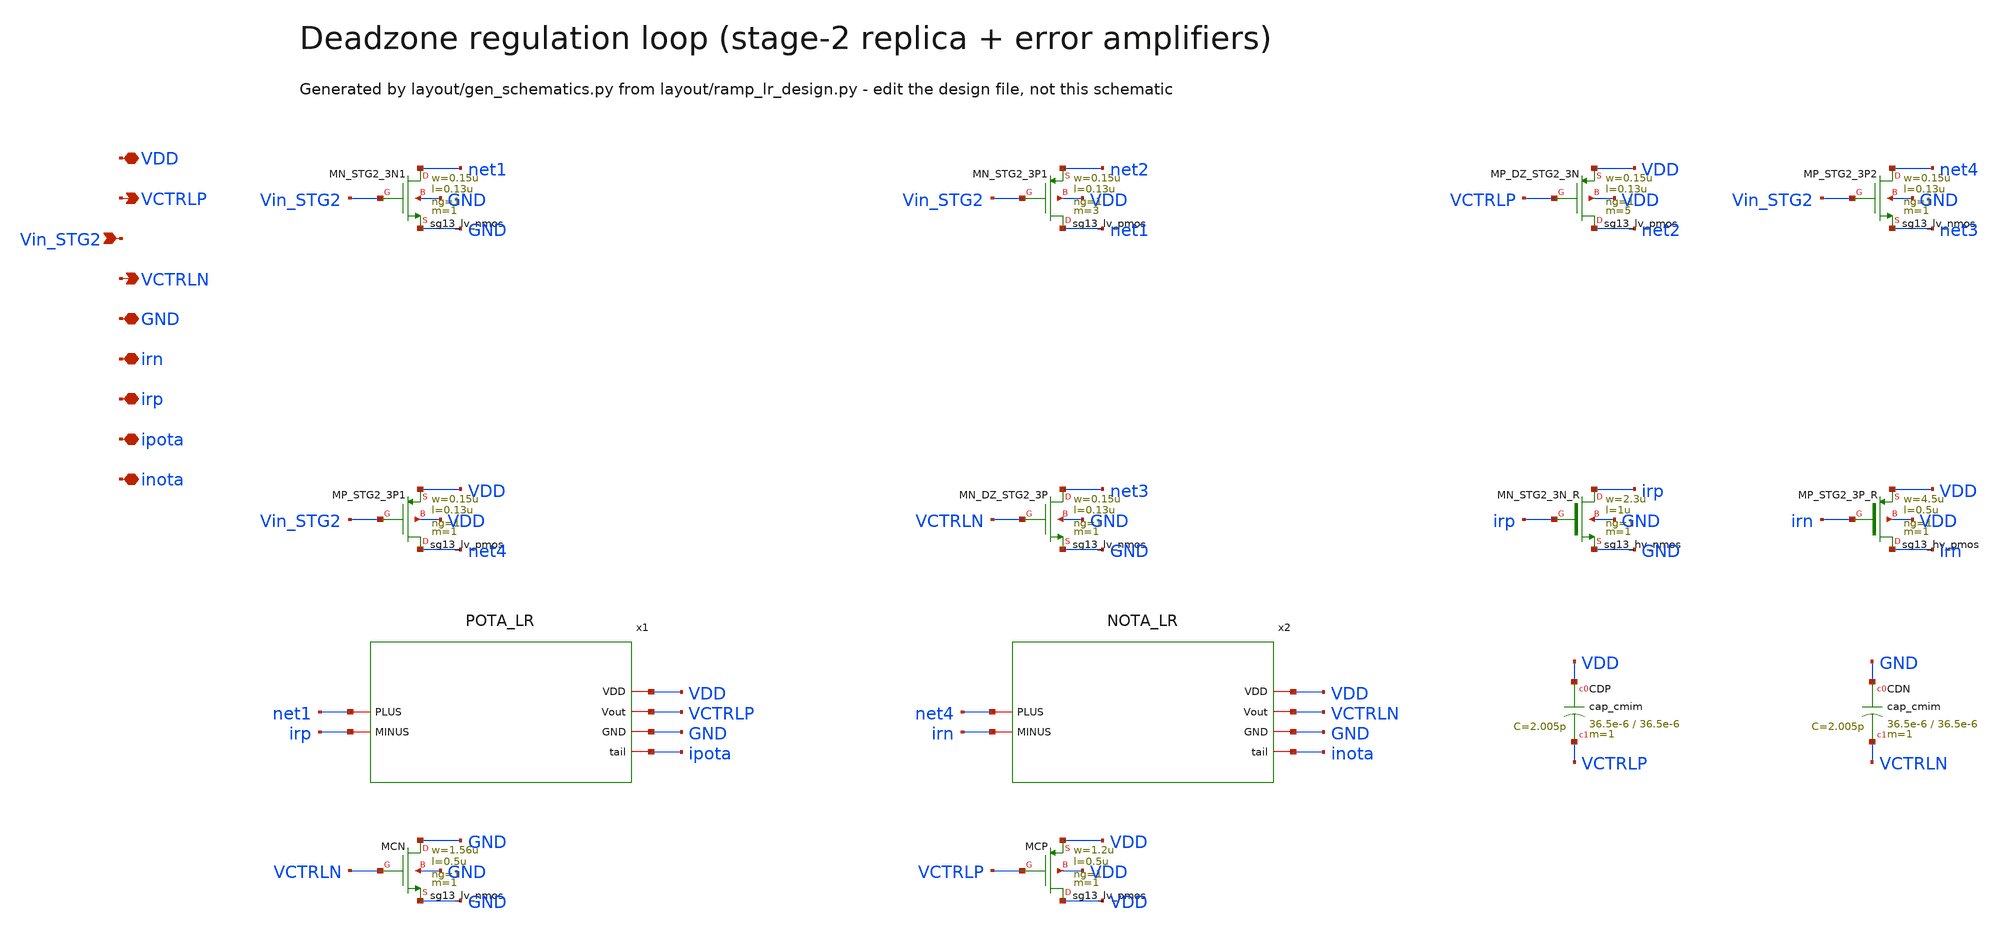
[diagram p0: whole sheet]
** sch_path: Design Files/RAMP/RAMP-LR/STG2_REPLICA_LR.sch
**.subckt STG2_REPLICA_LR VDD VCTRLP Vin_STG2 VCTRLN GND irn irp ipota inota
*.iopin VDD
*.opin VCTRLP
*.ipin Vin_STG2
*.opin VCTRLN
*.iopin GND
*.iopin irn
*.iopin irp
*.iopin ipota
*.iopin inota
XMN_STG2_3N1 net1 Vin_STG2 GND GND sg13_lv_nmos w=0.15u l=0.13u ng=1 m=1 mm_ok=1
XMN_STG2_3P1 net1 Vin_STG2 net2 VDD sg13_lv_pmos w=0.15u l=0.13u ng=1 m=3 mm_ok=1
XMP_DZ_STG2_3N net2 VCTRLP VDD VDD sg13_lv_pmos w=0.15u l=0.13u ng=1 m=5 mm_ok=1
XMP_STG2_3P2 net4 Vin_STG2 net3 GND sg13_lv_nmos w=0.15u l=0.13u ng=1 m=1 mm_ok=1
XMP_STG2_3P1 net4 Vin_STG2 VDD VDD sg13_lv_pmos w=0.15u l=0.13u ng=1 m=1 mm_ok=1
XMN_DZ_STG2_3P net3 VCTRLN GND GND sg13_lv_nmos w=0.15u l=0.13u ng=1 m=1 mm_ok=1
XMN_STG2_3N_R irp irp GND GND sg13_hv_nmos w=2.3u l=1u ng=1 m=1 mm_ok=1
XMP_STG2_3P_R irn irn VDD VDD sg13_hv_pmos w=4.5u l=0.5u ng=1 m=1 mm_ok=1
x1 VDD net1 irp VCTRLP GND ipota POTA_LR
x2 VDD VCTRLN net4 irn GND inota NOTA_LR
XCDP VDD VCTRLP cap_cmim w=36.5e-6 l=36.5e-6 m=1 mm_ok=1
XCDN GND VCTRLN cap_cmim w=36.5e-6 l=36.5e-6 m=1 mm_ok=1
XMCN GND VCTRLN GND GND sg13_lv_nmos w=1.56u l=0.5u ng=1 m=1 mm_ok=1
XMCP VDD VCTRLP VDD VDD sg13_lv_pmos w=1.2u l=0.5u ng=1 m=1 mm_ok=1
**.ends

* expanding   symbol:  RAMP-LR/POTA_LR.sym # of pins=6
** sym_path: Design Files/RAMP/RAMP-LR/POTA_LR.sym
** sch_path: Design Files/RAMP/RAMP-LR/POTA_LR.sch
.subckt POTA_LR VDD PLUS MINUS Vout GND tail
*.iopin VDD
*.ipin PLUS
*.ipin MINUS
*.opin Vout
*.iopin GND
*.iopin tail
XM2 net2 PLUS tail VDD sg13_lv_pmos w=1.2u l=0.5u ng=1 m=2 mm_ok=1
XM1 Vout MINUS tail VDD sg13_lv_pmos w=1.2u l=0.5u ng=1 m=2 mm_ok=1
XM4 Vout net2 GND GND sg13_hv_nmos w=0.5u l=2u ng=1 m=2 mm_ok=1
XM5 net2 net2 GND GND sg13_hv_nmos w=0.5u l=2u ng=1 m=2 mm_ok=1
.ends


* expanding   symbol:  RAMP-LR/NOTA_LR.sym # of pins=6
** sym_path: Design Files/RAMP/RAMP-LR/NOTA_LR.sym
** sch_path: Design Files/RAMP/RAMP-LR/NOTA_LR.sch
.subckt NOTA_LR VDD Vout PLUS MINUS GND tail
*.iopin VDD
*.opin Vout
*.ipin PLUS
*.ipin MINUS
*.iopin GND
*.iopin tail
XM1 net2 PLUS tail GND sg13_hv_nmos w=1.75u l=1u ng=1 m=2 mm_ok=1
XM2 Vout MINUS tail GND sg13_hv_nmos w=1.75u l=1u ng=1 m=2 mm_ok=1
XM3 Vout net2 VDD VDD sg13_hv_pmos w=0.5u l=0.75u ng=1 m=1 mm_ok=1
XM4 net2 net2 VDD VDD sg13_hv_pmos w=0.5u l=0.75u ng=1 m=1 mm_ok=1
.ends

.end
